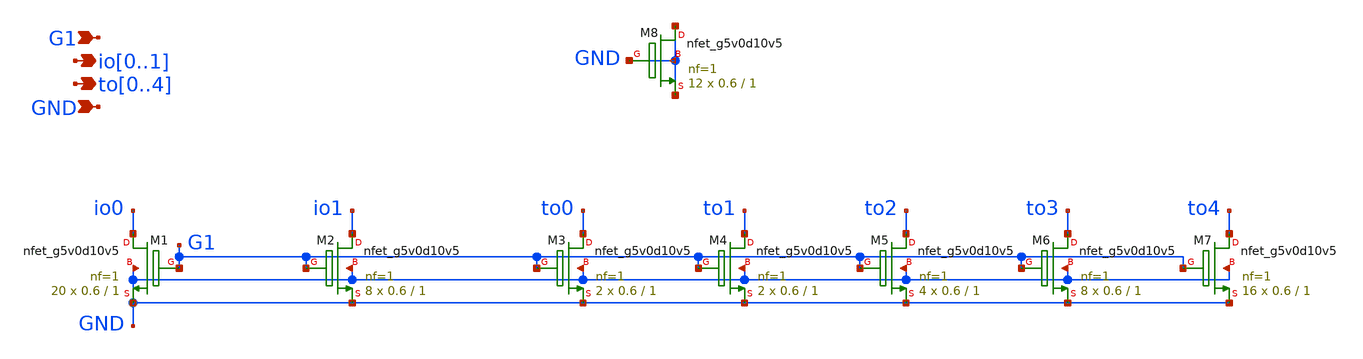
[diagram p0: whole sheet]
** sch_path: xschem/cm_ncell1.sch
**.subckt cm_ncell1 G1 io0,io1 GND to0,to1,to2,to3,to4
*.ipin G1
*.opin io0,io1
*.ipin GND
*.opin to0,to1,to2,to3,to4
XM1 io0 G1 GND GND sky130_fd_pr__nfet_g5v0d10v5 L=1 W=0.6 nf=1 ad='int((nf+1)/2) * W/nf * 0.29' as='int((nf+2)/2) * W/nf * 0.29'
+ pd='2*int((nf+1)/2) * (W/nf + 0.29)' ps='2*int((nf+2)/2) * (W/nf + 0.29)' nrd='0.29 / W' nrs='0.29 / W'
+ sa=0 sb=0 sd=0 mult=20 m=20
XM2 io1 G1 GND GND sky130_fd_pr__nfet_g5v0d10v5 L=1 W=0.6 nf=1 ad='int((nf+1)/2) * W/nf * 0.29' as='int((nf+2)/2) * W/nf * 0.29'
+ pd='2*int((nf+1)/2) * (W/nf + 0.29)' ps='2*int((nf+2)/2) * (W/nf + 0.29)' nrd='0.29 / W' nrs='0.29 / W'
+ sa=0 sb=0 sd=0 mult=8 m=8
XM3 to0 G1 GND GND sky130_fd_pr__nfet_g5v0d10v5 L=1 W=0.6 nf=1 ad='int((nf+1)/2) * W/nf * 0.29' as='int((nf+2)/2) * W/nf * 0.29'
+ pd='2*int((nf+1)/2) * (W/nf + 0.29)' ps='2*int((nf+2)/2) * (W/nf + 0.29)' nrd='0.29 / W' nrs='0.29 / W'
+ sa=0 sb=0 sd=0 mult=2 m=2
XM5 to2 G1 GND GND sky130_fd_pr__nfet_g5v0d10v5 L=1 W=0.6 nf=1 ad='int((nf+1)/2) * W/nf * 0.29' as='int((nf+2)/2) * W/nf * 0.29'
+ pd='2*int((nf+1)/2) * (W/nf + 0.29)' ps='2*int((nf+2)/2) * (W/nf + 0.29)' nrd='0.29 / W' nrs='0.29 / W'
+ sa=0 sb=0 sd=0 mult=4 m=4
XM6 to3 G1 GND GND sky130_fd_pr__nfet_g5v0d10v5 L=1 W=0.6 nf=1 ad='int((nf+1)/2) * W/nf * 0.29' as='int((nf+2)/2) * W/nf * 0.29'
+ pd='2*int((nf+1)/2) * (W/nf + 0.29)' ps='2*int((nf+2)/2) * (W/nf + 0.29)' nrd='0.29 / W' nrs='0.29 / W'
+ sa=0 sb=0 sd=0 mult=8 m=8
XM7 to4 G1 GND GND sky130_fd_pr__nfet_g5v0d10v5 L=1 W=0.6 nf=1 ad='int((nf+1)/2) * W/nf * 0.29' as='int((nf+2)/2) * W/nf * 0.29'
+ pd='2*int((nf+1)/2) * (W/nf + 0.29)' ps='2*int((nf+2)/2) * (W/nf + 0.29)' nrd='0.29 / W' nrs='0.29 / W'
+ sa=0 sb=0 sd=0 mult=16 m=16
XM4 to1 G1 GND GND sky130_fd_pr__nfet_g5v0d10v5 L=1 W=0.6 nf=1 ad='int((nf+1)/2) * W/nf * 0.29' as='int((nf+2)/2) * W/nf * 0.29'
+ pd='2*int((nf+1)/2) * (W/nf + 0.29)' ps='2*int((nf+2)/2) * (W/nf + 0.29)' nrd='0.29 / W' nrs='0.29 / W'
+ sa=0 sb=0 sd=0 mult=2 m=2
XM8 GND GND GND GND sky130_fd_pr__nfet_g5v0d10v5 L=1 W=0.6 nf=1 ad='int((nf+1)/2) * W/nf * 0.29' as='int((nf+2)/2) * W/nf * 0.29'
+ pd='2*int((nf+1)/2) * (W/nf + 0.29)' ps='2*int((nf+2)/2) * (W/nf + 0.29)' nrd='0.29 / W' nrs='0.29 / W'
+ sa=0 sb=0 sd=0 mult=12 m=12
**.ends
.end
